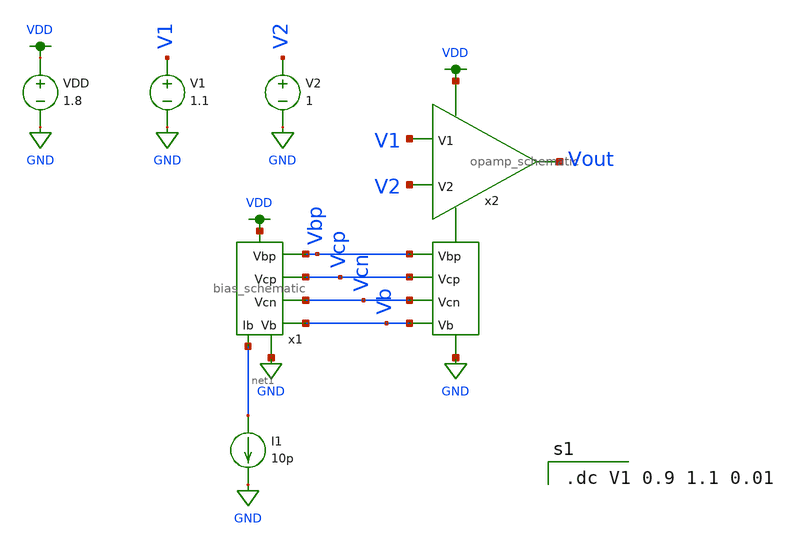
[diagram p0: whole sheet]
** sch_path: mp3/xschem/test_opamp.sch
**.subckt test_opamp
x1 VDD Vbp net1 Vcp Vcn GND Vb bias_schematic
x2 VDD Vbp Vcp Vout V1 V2 Vcn Vb GND opamp_schematic
I1 net1 GND 10p
V1 V1 GND 1.1
V2 V2 GND 1
VDD VDD GND 1.8
**** begin user architecture code

.option wnflag=1
.lib ~/skywater/skywater-pdk/libraries/sky130_fd_pr_ngspice/latest/models/sky130.lib.spice tt


.dc V1 0.9 1.1 0.01

**** end user architecture code
**.ends

* expanding   symbol:  /home/madvlsi/dev/git/vlsi/mp3/xschem/bias_schematic.sym # of pins=7
** sym_path: mp3/debug_files/bias_schematic.sym
** sch_path: mp3/debug_files/bias_schematic.sch
.subckt bias_schematic VP Vbp Ib Vcp Vcn VN Vb
*.iopin VP
*.iopin VN
*.iopin Ib
*.opin Vcp
*.opin Vbp
*.opin Vcn
*.opin Vb
XM1a net2 net2 net1 GND sky130_fd_pr__nfet_01v8 L=0.5 W=30 nf=1 ad='int((nf+1)/2) * W/nf * 0.29' as='int((nf+2)/2) * W/nf * 0.29'
+ pd='2*int((nf+1)/2) * (W/nf + 0.29)' ps='2*int((nf+2)/2) * (W/nf + 0.29)' nrd='0.29 / W' nrs='0.29 / W'
+ sa=0 sb=0 sd=0 mult=1 m=1
XM1b net2 net2 net1 GND sky130_fd_pr__nfet_01v8 L=0.5 W=30 nf=1 ad='int((nf+1)/2) * W/nf * 0.29' as='int((nf+2)/2) * W/nf * 0.29'
+ pd='2*int((nf+1)/2) * (W/nf + 0.29)' ps='2*int((nf+2)/2) * (W/nf + 0.29)' nrd='0.29 / W' nrs='0.29 / W'
+ sa=0 sb=0 sd=0 mult=1 m=1
XM1c net2 net2 net1 GND sky130_fd_pr__nfet_01v8 L=0.5 W=30 nf=1 ad='int((nf+1)/2) * W/nf * 0.29' as='int((nf+2)/2) * W/nf * 0.29'
+ pd='2*int((nf+1)/2) * (W/nf + 0.29)' ps='2*int((nf+2)/2) * (W/nf + 0.29)' nrd='0.29 / W' nrs='0.29 / W'
+ sa=0 sb=0 sd=0 mult=1 m=1
XM1d net2 net2 net1 GND sky130_fd_pr__nfet_01v8 L=0.5 W=30 nf=1 ad='int((nf+1)/2) * W/nf * 0.29' as='int((nf+2)/2) * W/nf * 0.29'
+ pd='2*int((nf+1)/2) * (W/nf + 0.29)' ps='2*int((nf+2)/2) * (W/nf + 0.29)' nrd='0.29 / W' nrs='0.29 / W'
+ sa=0 sb=0 sd=0 mult=1 m=1
XM2a VN net2 net1 GND sky130_fd_pr__nfet_01v8 L=0.5 W=3 nf=1 ad='int((nf+1)/2) * W/nf * 0.29' as='int((nf+2)/2) * W/nf * 0.29'
+ pd='2*int((nf+1)/2) * (W/nf + 0.29)' ps='2*int((nf+2)/2) * (W/nf + 0.29)' nrd='0.29 / W' nrs='0.29 / W'
+ sa=0 sb=0 sd=0 mult=1 m=1
XM2b VN net2 net1 GND sky130_fd_pr__nfet_01v8 L=0.5 W=3 nf=1 ad='int((nf+1)/2) * W/nf * 0.29' as='int((nf+2)/2) * W/nf * 0.29'
+ pd='2*int((nf+1)/2) * (W/nf + 0.29)' ps='2*int((nf+2)/2) * (W/nf + 0.29)' nrd='0.29 / W' nrs='0.29 / W'
+ sa=0 sb=0 sd=0 mult=1 m=1
XM2c VN net2 net1 GND sky130_fd_pr__nfet_01v8 L=0.5 W=3 nf=1 ad='int((nf+1)/2) * W/nf * 0.29' as='int((nf+2)/2) * W/nf * 0.29'
+ pd='2*int((nf+1)/2) * (W/nf + 0.29)' ps='2*int((nf+2)/2) * (W/nf + 0.29)' nrd='0.29 / W' nrs='0.29 / W'
+ sa=0 sb=0 sd=0 mult=1 m=1
XM2d VN net2 net1 GND sky130_fd_pr__nfet_01v8 L=0.5 W=3 nf=1 ad='int((nf+1)/2) * W/nf * 0.29' as='int((nf+2)/2) * W/nf * 0.29'
+ pd='2*int((nf+1)/2) * (W/nf + 0.29)' ps='2*int((nf+2)/2) * (W/nf + 0.29)' nrd='0.29 / W' nrs='0.29 / W'
+ sa=0 sb=0 sd=0 mult=1 m=1
XM3a net2 Ib VP VDD sky130_fd_pr__pfet_01v8 L=0.5 W=3 nf=1 ad='int((nf+1)/2) * W/nf * 0.29' as='int((nf+2)/2) * W/nf * 0.29'
+ pd='2*int((nf+1)/2) * (W/nf + 0.29)' ps='2*int((nf+2)/2) * (W/nf + 0.29)' nrd='0.29 / W' nrs='0.29 / W'
+ sa=0 sb=0 sd=0 mult=1 m=1
XM3b net2 Ib VP VDD sky130_fd_pr__pfet_01v8 L=0.5 W=3 nf=1 ad='int((nf+1)/2) * W/nf * 0.29' as='int((nf+2)/2) * W/nf * 0.29'
+ pd='2*int((nf+1)/2) * (W/nf + 0.29)' ps='2*int((nf+2)/2) * (W/nf + 0.29)' nrd='0.29 / W' nrs='0.29 / W'
+ sa=0 sb=0 sd=0 mult=1 m=1
XM3c net2 Ib VP VDD sky130_fd_pr__pfet_01v8 L=0.5 W=3 nf=1 ad='int((nf+1)/2) * W/nf * 0.29' as='int((nf+2)/2) * W/nf * 0.29'
+ pd='2*int((nf+1)/2) * (W/nf + 0.29)' ps='2*int((nf+2)/2) * (W/nf + 0.29)' nrd='0.29 / W' nrs='0.29 / W'
+ sa=0 sb=0 sd=0 mult=1 m=1
XM3d net2 Ib VP VDD sky130_fd_pr__pfet_01v8 L=0.5 W=3 nf=1 ad='int((nf+1)/2) * W/nf * 0.29' as='int((nf+2)/2) * W/nf * 0.29'
+ pd='2*int((nf+1)/2) * (W/nf + 0.29)' ps='2*int((nf+2)/2) * (W/nf + 0.29)' nrd='0.29 / W' nrs='0.29 / W'
+ sa=0 sb=0 sd=0 mult=1 m=1
XM4a Vcn Ib VP VDD sky130_fd_pr__pfet_01v8 L=0.5 W=30 nf=1 ad='int((nf+1)/2) * W/nf * 0.29' as='int((nf+2)/2) * W/nf * 0.29'
+ pd='2*int((nf+1)/2) * (W/nf + 0.29)' ps='2*int((nf+2)/2) * (W/nf + 0.29)' nrd='0.29 / W' nrs='0.29 / W'
+ sa=0 sb=0 sd=0 mult=1 m=1
XM4b Vcn Ib VP VDD sky130_fd_pr__pfet_01v8 L=0.5 W=30 nf=1 ad='int((nf+1)/2) * W/nf * 0.29' as='int((nf+2)/2) * W/nf * 0.29'
+ pd='2*int((nf+1)/2) * (W/nf + 0.29)' ps='2*int((nf+2)/2) * (W/nf + 0.29)' nrd='0.29 / W' nrs='0.29 / W'
+ sa=0 sb=0 sd=0 mult=1 m=1
XM4c Vcn Ib VP VDD sky130_fd_pr__pfet_01v8 L=0.5 W=30 nf=1 ad='int((nf+1)/2) * W/nf * 0.29' as='int((nf+2)/2) * W/nf * 0.29'
+ pd='2*int((nf+1)/2) * (W/nf + 0.29)' ps='2*int((nf+2)/2) * (W/nf + 0.29)' nrd='0.29 / W' nrs='0.29 / W'
+ sa=0 sb=0 sd=0 mult=1 m=1
XM4d Vcn Ib VP VDD sky130_fd_pr__pfet_01v8 L=0.5 W=30 nf=1 ad='int((nf+1)/2) * W/nf * 0.29' as='int((nf+2)/2) * W/nf * 0.29'
+ pd='2*int((nf+1)/2) * (W/nf + 0.29)' ps='2*int((nf+2)/2) * (W/nf + 0.29)' nrd='0.29 / W' nrs='0.29 / W'
+ sa=0 sb=0 sd=0 mult=1 m=1
XM11a Ib Ib VP VDD sky130_fd_pr__pfet_01v8 L=0.5 W=3 nf=1 ad='int((nf+1)/2) * W/nf * 0.29' as='int((nf+2)/2) * W/nf * 0.29'
+ pd='2*int((nf+1)/2) * (W/nf + 0.29)' ps='2*int((nf+2)/2) * (W/nf + 0.29)' nrd='0.29 / W' nrs='0.29 / W'
+ sa=0 sb=0 sd=0 mult=1 m=1
XM11b Ib Ib VP VDD sky130_fd_pr__pfet_01v8 L=0.5 W=3 nf=1 ad='int((nf+1)/2) * W/nf * 0.29' as='int((nf+2)/2) * W/nf * 0.29'
+ pd='2*int((nf+1)/2) * (W/nf + 0.29)' ps='2*int((nf+2)/2) * (W/nf + 0.29)' nrd='0.29 / W' nrs='0.29 / W'
+ sa=0 sb=0 sd=0 mult=1 m=1
XM11c Ib Ib VP VDD sky130_fd_pr__pfet_01v8 L=0.5 W=3 nf=1 ad='int((nf+1)/2) * W/nf * 0.29' as='int((nf+2)/2) * W/nf * 0.29'
+ pd='2*int((nf+1)/2) * (W/nf + 0.29)' ps='2*int((nf+2)/2) * (W/nf + 0.29)' nrd='0.29 / W' nrs='0.29 / W'
+ sa=0 sb=0 sd=0 mult=1 m=1
XM11d Ib Ib VP VDD sky130_fd_pr__pfet_01v8 L=0.5 W=3 nf=1 ad='int((nf+1)/2) * W/nf * 0.29' as='int((nf+2)/2) * W/nf * 0.29'
+ pd='2*int((nf+1)/2) * (W/nf + 0.29)' ps='2*int((nf+2)/2) * (W/nf + 0.29)' nrd='0.29 / W' nrs='0.29 / W'
+ sa=0 sb=0 sd=0 mult=1 m=1
XM5a net1 Vcn Vcn GND sky130_fd_pr__nfet_01v8 L=0.5 W=30 nf=1 ad='int((nf+1)/2) * W/nf * 0.29' as='int((nf+2)/2) * W/nf * 0.29'
+ pd='2*int((nf+1)/2) * (W/nf + 0.29)' ps='2*int((nf+2)/2) * (W/nf + 0.29)' nrd='0.29 / W' nrs='0.29 / W'
+ sa=0 sb=0 sd=0 mult=1 m=1
XM5b net1 Vcn Vcn GND sky130_fd_pr__nfet_01v8 L=0.5 W=30 nf=1 ad='int((nf+1)/2) * W/nf * 0.29' as='int((nf+2)/2) * W/nf * 0.29'
+ pd='2*int((nf+1)/2) * (W/nf + 0.29)' ps='2*int((nf+2)/2) * (W/nf + 0.29)' nrd='0.29 / W' nrs='0.29 / W'
+ sa=0 sb=0 sd=0 mult=1 m=1
XM5c net1 Vcn Vcn GND sky130_fd_pr__nfet_01v8 L=0.5 W=30 nf=1 ad='int((nf+1)/2) * W/nf * 0.29' as='int((nf+2)/2) * W/nf * 0.29'
+ pd='2*int((nf+1)/2) * (W/nf + 0.29)' ps='2*int((nf+2)/2) * (W/nf + 0.29)' nrd='0.29 / W' nrs='0.29 / W'
+ sa=0 sb=0 sd=0 mult=1 m=1
XM5d net1 Vcn Vcn GND sky130_fd_pr__nfet_01v8 L=0.5 W=30 nf=1 ad='int((nf+1)/2) * W/nf * 0.29' as='int((nf+2)/2) * W/nf * 0.29'
+ pd='2*int((nf+1)/2) * (W/nf + 0.29)' ps='2*int((nf+2)/2) * (W/nf + 0.29)' nrd='0.29 / W' nrs='0.29 / W'
+ sa=0 sb=0 sd=0 mult=1 m=1
XM8a VN Vb net3 GND sky130_fd_pr__nfet_01v8 L=0.5 W=3 nf=1 ad='int((nf+1)/2) * W/nf * 0.29' as='int((nf+2)/2) * W/nf * 0.29'
+ pd='2*int((nf+1)/2) * (W/nf + 0.29)' ps='2*int((nf+2)/2) * (W/nf + 0.29)' nrd='0.29 / W' nrs='0.29 / W'
+ sa=0 sb=0 sd=0 mult=1 m=1
XM8b VN Vb net3 GND sky130_fd_pr__nfet_01v8 L=0.5 W=3 nf=1 ad='int((nf+1)/2) * W/nf * 0.29' as='int((nf+2)/2) * W/nf * 0.29'
+ pd='2*int((nf+1)/2) * (W/nf + 0.29)' ps='2*int((nf+2)/2) * (W/nf + 0.29)' nrd='0.29 / W' nrs='0.29 / W'
+ sa=0 sb=0 sd=0 mult=1 m=1
XM8c VN Vb net3 GND sky130_fd_pr__nfet_01v8 L=0.5 W=3 nf=1 ad='int((nf+1)/2) * W/nf * 0.29' as='int((nf+2)/2) * W/nf * 0.29'
+ pd='2*int((nf+1)/2) * (W/nf + 0.29)' ps='2*int((nf+2)/2) * (W/nf + 0.29)' nrd='0.29 / W' nrs='0.29 / W'
+ sa=0 sb=0 sd=0 mult=1 m=1
XM8d VN Vb net3 GND sky130_fd_pr__nfet_01v8 L=0.5 W=3 nf=1 ad='int((nf+1)/2) * W/nf * 0.29' as='int((nf+2)/2) * W/nf * 0.29'
+ pd='2*int((nf+1)/2) * (W/nf + 0.29)' ps='2*int((nf+2)/2) * (W/nf + 0.29)' nrd='0.29 / W' nrs='0.29 / W'
+ sa=0 sb=0 sd=0 mult=1 m=1
XM6a net3 net3 net4 VDD sky130_fd_pr__pfet_01v8 L=0.5 W=30 nf=1 ad='int((nf+1)/2) * W/nf * 0.29' as='int((nf+2)/2) * W/nf * 0.29'
+ pd='2*int((nf+1)/2) * (W/nf + 0.29)' ps='2*int((nf+2)/2) * (W/nf + 0.29)' nrd='0.29 / W' nrs='0.29 / W'
+ sa=0 sb=0 sd=0 mult=1 m=1
XM6b net3 net3 net4 VDD sky130_fd_pr__pfet_01v8 L=0.5 W=30 nf=1 ad='int((nf+1)/2) * W/nf * 0.29' as='int((nf+2)/2) * W/nf * 0.29'
+ pd='2*int((nf+1)/2) * (W/nf + 0.29)' ps='2*int((nf+2)/2) * (W/nf + 0.29)' nrd='0.29 / W' nrs='0.29 / W'
+ sa=0 sb=0 sd=0 mult=1 m=1
XM6c net3 net3 net4 VDD sky130_fd_pr__pfet_01v8 L=0.5 W=30 nf=1 ad='int((nf+1)/2) * W/nf * 0.29' as='int((nf+2)/2) * W/nf * 0.29'
+ pd='2*int((nf+1)/2) * (W/nf + 0.29)' ps='2*int((nf+2)/2) * (W/nf + 0.29)' nrd='0.29 / W' nrs='0.29 / W'
+ sa=0 sb=0 sd=0 mult=1 m=1
XM6d net3 net3 net4 VDD sky130_fd_pr__pfet_01v8 L=0.5 W=30 nf=1 ad='int((nf+1)/2) * W/nf * 0.29' as='int((nf+2)/2) * W/nf * 0.29'
+ pd='2*int((nf+1)/2) * (W/nf + 0.29)' ps='2*int((nf+2)/2) * (W/nf + 0.29)' nrd='0.29 / W' nrs='0.29 / W'
+ sa=0 sb=0 sd=0 mult=1 m=1
XM7a net4 net3 VP VDD sky130_fd_pr__pfet_01v8 L=0.5 W=3 nf=1 ad='int((nf+1)/2) * W/nf * 0.29' as='int((nf+2)/2) * W/nf * 0.29'
+ pd='2*int((nf+1)/2) * (W/nf + 0.29)' ps='2*int((nf+2)/2) * (W/nf + 0.29)' nrd='0.29 / W' nrs='0.29 / W'
+ sa=0 sb=0 sd=0 mult=1 m=1
XM7b net4 net3 VP VDD sky130_fd_pr__pfet_01v8 L=0.5 W=3 nf=1 ad='int((nf+1)/2) * W/nf * 0.29' as='int((nf+2)/2) * W/nf * 0.29'
+ pd='2*int((nf+1)/2) * (W/nf + 0.29)' ps='2*int((nf+2)/2) * (W/nf + 0.29)' nrd='0.29 / W' nrs='0.29 / W'
+ sa=0 sb=0 sd=0 mult=1 m=1
XM7c net4 net3 VP VDD sky130_fd_pr__pfet_01v8 L=0.5 W=3 nf=1 ad='int((nf+1)/2) * W/nf * 0.29' as='int((nf+2)/2) * W/nf * 0.29'
+ pd='2*int((nf+1)/2) * (W/nf + 0.29)' ps='2*int((nf+2)/2) * (W/nf + 0.29)' nrd='0.29 / W' nrs='0.29 / W'
+ sa=0 sb=0 sd=0 mult=1 m=1
XM7d net4 net3 VP VDD sky130_fd_pr__pfet_01v8 L=0.5 W=3 nf=1 ad='int((nf+1)/2) * W/nf * 0.29' as='int((nf+2)/2) * W/nf * 0.29'
+ pd='2*int((nf+1)/2) * (W/nf + 0.29)' ps='2*int((nf+2)/2) * (W/nf + 0.29)' nrd='0.29 / W' nrs='0.29 / W'
+ sa=0 sb=0 sd=0 mult=1 m=1
XM10d net4 Vcp Vcp VDD sky130_fd_pr__pfet_01v8 L=0.5 W=30 nf=1 ad='int((nf+1)/2) * W/nf * 0.29' as='int((nf+2)/2) * W/nf * 0.29'
+ pd='2*int((nf+1)/2) * (W/nf + 0.29)' ps='2*int((nf+2)/2) * (W/nf + 0.29)' nrd='0.29 / W' nrs='0.29 / W'
+ sa=0 sb=0 sd=0 mult=1 m=1
XM10c net4 Vcp Vcp VDD sky130_fd_pr__pfet_01v8 L=0.5 W=30 nf=1 ad='int((nf+1)/2) * W/nf * 0.29' as='int((nf+2)/2) * W/nf * 0.29'
+ pd='2*int((nf+1)/2) * (W/nf + 0.29)' ps='2*int((nf+2)/2) * (W/nf + 0.29)' nrd='0.29 / W' nrs='0.29 / W'
+ sa=0 sb=0 sd=0 mult=1 m=1
XM10b net4 Vcp Vcp VDD sky130_fd_pr__pfet_01v8 L=0.5 W=30 nf=1 ad='int((nf+1)/2) * W/nf * 0.29' as='int((nf+2)/2) * W/nf * 0.29'
+ pd='2*int((nf+1)/2) * (W/nf + 0.29)' ps='2*int((nf+2)/2) * (W/nf + 0.29)' nrd='0.29 / W' nrs='0.29 / W'
+ sa=0 sb=0 sd=0 mult=1 m=1
XM10a net4 Vcp Vcp VDD sky130_fd_pr__pfet_01v8 L=0.5 W=30 nf=1 ad='int((nf+1)/2) * W/nf * 0.29' as='int((nf+2)/2) * W/nf * 0.29'
+ pd='2*int((nf+1)/2) * (W/nf + 0.29)' ps='2*int((nf+2)/2) * (W/nf + 0.29)' nrd='0.29 / W' nrs='0.29 / W'
+ sa=0 sb=0 sd=0 mult=1 m=1
XM9a VN Vb Vcp GND sky130_fd_pr__nfet_01v8 L=0.5 W=30 nf=1 ad='int((nf+1)/2) * W/nf * 0.29' as='int((nf+2)/2) * W/nf * 0.29'
+ pd='2*int((nf+1)/2) * (W/nf + 0.29)' ps='2*int((nf+2)/2) * (W/nf + 0.29)' nrd='0.29 / W' nrs='0.29 / W'
+ sa=0 sb=0 sd=0 mult=1 m=1
XM9b VN Vb Vcp GND sky130_fd_pr__nfet_01v8 L=0.5 W=30 nf=1 ad='int((nf+1)/2) * W/nf * 0.29' as='int((nf+2)/2) * W/nf * 0.29'
+ pd='2*int((nf+1)/2) * (W/nf + 0.29)' ps='2*int((nf+2)/2) * (W/nf + 0.29)' nrd='0.29 / W' nrs='0.29 / W'
+ sa=0 sb=0 sd=0 mult=1 m=1
XM9c VN Vb Vcp GND sky130_fd_pr__nfet_01v8 L=0.5 W=30 nf=1 ad='int((nf+1)/2) * W/nf * 0.29' as='int((nf+2)/2) * W/nf * 0.29'
+ pd='2*int((nf+1)/2) * (W/nf + 0.29)' ps='2*int((nf+2)/2) * (W/nf + 0.29)' nrd='0.29 / W' nrs='0.29 / W'
+ sa=0 sb=0 sd=0 mult=1 m=1
XM9d VN Vb Vcp GND sky130_fd_pr__nfet_01v8 L=0.5 W=30 nf=1 ad='int((nf+1)/2) * W/nf * 0.29' as='int((nf+2)/2) * W/nf * 0.29'
+ pd='2*int((nf+1)/2) * (W/nf + 0.29)' ps='2*int((nf+2)/2) * (W/nf + 0.29)' nrd='0.29 / W' nrs='0.29 / W'
+ sa=0 sb=0 sd=0 mult=1 m=1
XM12a VN Vb Vb GND sky130_fd_pr__nfet_01v8 L=0.5 W=3 nf=1 ad='int((nf+1)/2) * W/nf * 0.29' as='int((nf+2)/2) * W/nf * 0.29'
+ pd='2*int((nf+1)/2) * (W/nf + 0.29)' ps='2*int((nf+2)/2) * (W/nf + 0.29)' nrd='0.29 / W' nrs='0.29 / W'
+ sa=0 sb=0 sd=0 mult=1 m=1
XM12b VN Vb Vb GND sky130_fd_pr__nfet_01v8 L=0.5 W=3 nf=1 ad='int((nf+1)/2) * W/nf * 0.29' as='int((nf+2)/2) * W/nf * 0.29'
+ pd='2*int((nf+1)/2) * (W/nf + 0.29)' ps='2*int((nf+2)/2) * (W/nf + 0.29)' nrd='0.29 / W' nrs='0.29 / W'
+ sa=0 sb=0 sd=0 mult=1 m=1
XM12c VN Vb Vb GND sky130_fd_pr__nfet_01v8 L=0.5 W=3 nf=1 ad='int((nf+1)/2) * W/nf * 0.29' as='int((nf+2)/2) * W/nf * 0.29'
+ pd='2*int((nf+1)/2) * (W/nf + 0.29)' ps='2*int((nf+2)/2) * (W/nf + 0.29)' nrd='0.29 / W' nrs='0.29 / W'
+ sa=0 sb=0 sd=0 mult=1 m=1
XM12d VN Vb Vb GND sky130_fd_pr__nfet_01v8 L=0.5 W=3 nf=1 ad='int((nf+1)/2) * W/nf * 0.29' as='int((nf+2)/2) * W/nf * 0.29'
+ pd='2*int((nf+1)/2) * (W/nf + 0.29)' ps='2*int((nf+2)/2) * (W/nf + 0.29)' nrd='0.29 / W' nrs='0.29 / W'
+ sa=0 sb=0 sd=0 mult=1 m=1
XM1 Vb Ib VP VDD sky130_fd_pr__pfet_01v8 L=0.5 W=3 nf=1 ad='int((nf+1)/2) * W/nf * 0.29' as='int((nf+2)/2) * W/nf * 0.29'
+ pd='2*int((nf+1)/2) * (W/nf + 0.29)' ps='2*int((nf+2)/2) * (W/nf + 0.29)' nrd='0.29 / W' nrs='0.29 / W'
+ sa=0 sb=0 sd=0 mult=1 m=1
XM2 Vb Ib VP VDD sky130_fd_pr__pfet_01v8 L=0.5 W=3 nf=1 ad='int((nf+1)/2) * W/nf * 0.29' as='int((nf+2)/2) * W/nf * 0.29'
+ pd='2*int((nf+1)/2) * (W/nf + 0.29)' ps='2*int((nf+2)/2) * (W/nf + 0.29)' nrd='0.29 / W' nrs='0.29 / W'
+ sa=0 sb=0 sd=0 mult=1 m=1
XM3 Vb Ib VP VDD sky130_fd_pr__pfet_01v8 L=0.5 W=3 nf=1 ad='int((nf+1)/2) * W/nf * 0.29' as='int((nf+2)/2) * W/nf * 0.29'
+ pd='2*int((nf+1)/2) * (W/nf + 0.29)' ps='2*int((nf+2)/2) * (W/nf + 0.29)' nrd='0.29 / W' nrs='0.29 / W'
+ sa=0 sb=0 sd=0 mult=1 m=1
XM4 Vb Ib VP VDD sky130_fd_pr__pfet_01v8 L=0.5 W=3 nf=1 ad='int((nf+1)/2) * W/nf * 0.29' as='int((nf+2)/2) * W/nf * 0.29'
+ pd='2*int((nf+1)/2) * (W/nf + 0.29)' ps='2*int((nf+2)/2) * (W/nf + 0.29)' nrd='0.29 / W' nrs='0.29 / W'
+ sa=0 sb=0 sd=0 mult=1 m=1
.ends


* expanding   symbol:  /home/madvlsi/dev/git/vlsi/mp3/xschem/opamp_schematic.sym # of pins=9
** sym_path: /home/madvlsi/dev/git/vlsi/mp3/xschem/opamp_schematic.sym
** sch_path: /home/madvlsi/dev/git/vlsi/mp3/xschem/opamp_schematic.sch
.subckt opamp_schematic VP Vbp Vcp Vout V1 V2 Vcn Vb VN
*.ipin Vbp
*.ipin Vcp
*.ipin Vcn
*.ipin V2
*.ipin V1
*.ipin Vb
*.iopin VP
*.iopin VN
*.opin Vout
XM1a net2 V1 net1 GND sky130_fd_pr__nfet_01v8 L=0.5 W=3 nf=1 ad='int((nf+1)/2) * W/nf * 0.29' as='int((nf+2)/2) * W/nf * 0.29'
+ pd='2*int((nf+1)/2) * (W/nf + 0.29)' ps='2*int((nf+2)/2) * (W/nf + 0.29)' nrd='0.29 / W' nrs='0.29 / W'
+ sa=0 sb=0 sd=0 mult=1 m=1
XM1b net2 V1 net1 GND sky130_fd_pr__nfet_01v8 L=0.5 W=3 nf=1 ad='int((nf+1)/2) * W/nf * 0.29' as='int((nf+2)/2) * W/nf * 0.29'
+ pd='2*int((nf+1)/2) * (W/nf + 0.29)' ps='2*int((nf+2)/2) * (W/nf + 0.29)' nrd='0.29 / W' nrs='0.29 / W'
+ sa=0 sb=0 sd=0 mult=1 m=1
XM1c net2 V1 net1 GND sky130_fd_pr__nfet_01v8 L=0.5 W=3 nf=1 ad='int((nf+1)/2) * W/nf * 0.29' as='int((nf+2)/2) * W/nf * 0.29'
+ pd='2*int((nf+1)/2) * (W/nf + 0.29)' ps='2*int((nf+2)/2) * (W/nf + 0.29)' nrd='0.29 / W' nrs='0.29 / W'
+ sa=0 sb=0 sd=0 mult=1 m=1
XM1d net2 V1 net1 GND sky130_fd_pr__nfet_01v8 L=0.5 W=3 nf=1 ad='int((nf+1)/2) * W/nf * 0.29' as='int((nf+2)/2) * W/nf * 0.29'
+ pd='2*int((nf+1)/2) * (W/nf + 0.29)' ps='2*int((nf+2)/2) * (W/nf + 0.29)' nrd='0.29 / W' nrs='0.29 / W'
+ sa=0 sb=0 sd=0 mult=1 m=1
XM2a net3 V2 net1 GND sky130_fd_pr__nfet_01v8 L=0.5 W=3 nf=1 ad='int((nf+1)/2) * W/nf * 0.29' as='int((nf+2)/2) * W/nf * 0.29'
+ pd='2*int((nf+1)/2) * (W/nf + 0.29)' ps='2*int((nf+2)/2) * (W/nf + 0.29)' nrd='0.29 / W' nrs='0.29 / W'
+ sa=0 sb=0 sd=0 mult=1 m=1
XM2b net3 V2 net1 GND sky130_fd_pr__nfet_01v8 L=0.5 W=3 nf=1 ad='int((nf+1)/2) * W/nf * 0.29' as='int((nf+2)/2) * W/nf * 0.29'
+ pd='2*int((nf+1)/2) * (W/nf + 0.29)' ps='2*int((nf+2)/2) * (W/nf + 0.29)' nrd='0.29 / W' nrs='0.29 / W'
+ sa=0 sb=0 sd=0 mult=1 m=1
XM2c net3 V2 net1 GND sky130_fd_pr__nfet_01v8 L=0.5 W=3 nf=1 ad='int((nf+1)/2) * W/nf * 0.29' as='int((nf+2)/2) * W/nf * 0.29'
+ pd='2*int((nf+1)/2) * (W/nf + 0.29)' ps='2*int((nf+2)/2) * (W/nf + 0.29)' nrd='0.29 / W' nrs='0.29 / W'
+ sa=0 sb=0 sd=0 mult=1 m=1
XM2d net3 V2 net1 GND sky130_fd_pr__nfet_01v8 L=0.5 W=3 nf=1 ad='int((nf+1)/2) * W/nf * 0.29' as='int((nf+2)/2) * W/nf * 0.29'
+ pd='2*int((nf+1)/2) * (W/nf + 0.29)' ps='2*int((nf+2)/2) * (W/nf + 0.29)' nrd='0.29 / W' nrs='0.29 / W'
+ sa=0 sb=0 sd=0 mult=1 m=1
XMba net1 Vb VN GND sky130_fd_pr__nfet_01v8 L=0.5 W=1.5 nf=1 ad='int((nf+1)/2) * W/nf * 0.29' as='int((nf+2)/2) * W/nf * 0.29'
+ pd='2*int((nf+1)/2) * (W/nf + 0.29)' ps='2*int((nf+2)/2) * (W/nf + 0.29)' nrd='0.29 / W' nrs='0.29 / W'
+ sa=0 sb=0 sd=0 mult=1 m=1
XMbb net1 Vb VN GND sky130_fd_pr__nfet_01v8 L=0.5 W=1.5 nf=1 ad='int((nf+1)/2) * W/nf * 0.29' as='int((nf+2)/2) * W/nf * 0.29'
+ pd='2*int((nf+1)/2) * (W/nf + 0.29)' ps='2*int((nf+2)/2) * (W/nf + 0.29)' nrd='0.29 / W' nrs='0.29 / W'
+ sa=0 sb=0 sd=0 mult=1 m=1
XMbc net1 Vb VN GND sky130_fd_pr__nfet_01v8 L=0.5 W=1.5 nf=1 ad='int((nf+1)/2) * W/nf * 0.29' as='int((nf+2)/2) * W/nf * 0.29'
+ pd='2*int((nf+1)/2) * (W/nf + 0.29)' ps='2*int((nf+2)/2) * (W/nf + 0.29)' nrd='0.29 / W' nrs='0.29 / W'
+ sa=0 sb=0 sd=0 mult=1 m=1
XMbd net1 Vb VN GND sky130_fd_pr__nfet_01v8 L=0.5 W=1.5 nf=1 ad='int((nf+1)/2) * W/nf * 0.29' as='int((nf+2)/2) * W/nf * 0.29'
+ pd='2*int((nf+1)/2) * (W/nf + 0.29)' ps='2*int((nf+2)/2) * (W/nf + 0.29)' nrd='0.29 / W' nrs='0.29 / W'
+ sa=0 sb=0 sd=0 mult=1 m=1
XMbe net1 Vb VN GND sky130_fd_pr__nfet_01v8 L=0.5 W=1.5 nf=1 ad='int((nf+1)/2) * W/nf * 0.29' as='int((nf+2)/2) * W/nf * 0.29'
+ pd='2*int((nf+1)/2) * (W/nf + 0.29)' ps='2*int((nf+2)/2) * (W/nf + 0.29)' nrd='0.29 / W' nrs='0.29 / W'
+ sa=0 sb=0 sd=0 mult=1 m=1
XMbf net1 Vb VN GND sky130_fd_pr__nfet_01v8 L=0.5 W=1.5 nf=1 ad='int((nf+1)/2) * W/nf * 0.29' as='int((nf+2)/2) * W/nf * 0.29'
+ pd='2*int((nf+1)/2) * (W/nf + 0.29)' ps='2*int((nf+2)/2) * (W/nf + 0.29)' nrd='0.29 / W' nrs='0.29 / W'
+ sa=0 sb=0 sd=0 mult=1 m=1
XMbg net1 Vb VN GND sky130_fd_pr__nfet_01v8 L=0.5 W=1.5 nf=1 ad='int((nf+1)/2) * W/nf * 0.29' as='int((nf+2)/2) * W/nf * 0.29'
+ pd='2*int((nf+1)/2) * (W/nf + 0.29)' ps='2*int((nf+2)/2) * (W/nf + 0.29)' nrd='0.29 / W' nrs='0.29 / W'
+ sa=0 sb=0 sd=0 mult=1 m=1
XMbh net1 Vb VN GND sky130_fd_pr__nfet_01v8 L=0.5 W=1.5 nf=1 ad='int((nf+1)/2) * W/nf * 0.29' as='int((nf+2)/2) * W/nf * 0.29'
+ pd='2*int((nf+1)/2) * (W/nf + 0.29)' ps='2*int((nf+2)/2) * (W/nf + 0.29)' nrd='0.29 / W' nrs='0.29 / W'
+ sa=0 sb=0 sd=0 mult=1 m=1
XM7a net5 Vcn net4 GND sky130_fd_pr__nfet_01v8 L=0.5 W=3 nf=1 ad='int((nf+1)/2) * W/nf * 0.29' as='int((nf+2)/2) * W/nf * 0.29'
+ pd='2*int((nf+1)/2) * (W/nf + 0.29)' ps='2*int((nf+2)/2) * (W/nf + 0.29)' nrd='0.29 / W' nrs='0.29 / W'
+ sa=0 sb=0 sd=0 mult=1 m=1
XM7b net5 Vcn net4 GND sky130_fd_pr__nfet_01v8 L=0.5 W=3 nf=1 ad='int((nf+1)/2) * W/nf * 0.29' as='int((nf+2)/2) * W/nf * 0.29'
+ pd='2*int((nf+1)/2) * (W/nf + 0.29)' ps='2*int((nf+2)/2) * (W/nf + 0.29)' nrd='0.29 / W' nrs='0.29 / W'
+ sa=0 sb=0 sd=0 mult=1 m=1
XM7c net5 Vcn net4 GND sky130_fd_pr__nfet_01v8 L=0.5 W=3 nf=1 ad='int((nf+1)/2) * W/nf * 0.29' as='int((nf+2)/2) * W/nf * 0.29'
+ pd='2*int((nf+1)/2) * (W/nf + 0.29)' ps='2*int((nf+2)/2) * (W/nf + 0.29)' nrd='0.29 / W' nrs='0.29 / W'
+ sa=0 sb=0 sd=0 mult=1 m=1
XM7d net5 Vcn net4 GND sky130_fd_pr__nfet_01v8 L=0.5 W=3 nf=1 ad='int((nf+1)/2) * W/nf * 0.29' as='int((nf+2)/2) * W/nf * 0.29'
+ pd='2*int((nf+1)/2) * (W/nf + 0.29)' ps='2*int((nf+2)/2) * (W/nf + 0.29)' nrd='0.29 / W' nrs='0.29 / W'
+ sa=0 sb=0 sd=0 mult=1 m=1
XM8a net6 Vcn Vout GND sky130_fd_pr__nfet_01v8 L=0.5 W=3 nf=1 ad='int((nf+1)/2) * W/nf * 0.29' as='int((nf+2)/2) * W/nf * 0.29'
+ pd='2*int((nf+1)/2) * (W/nf + 0.29)' ps='2*int((nf+2)/2) * (W/nf + 0.29)' nrd='0.29 / W' nrs='0.29 / W'
+ sa=0 sb=0 sd=0 mult=1 m=1
XM8b net6 Vcn Vout GND sky130_fd_pr__nfet_01v8 L=0.5 W=3 nf=1 ad='int((nf+1)/2) * W/nf * 0.29' as='int((nf+2)/2) * W/nf * 0.29'
+ pd='2*int((nf+1)/2) * (W/nf + 0.29)' ps='2*int((nf+2)/2) * (W/nf + 0.29)' nrd='0.29 / W' nrs='0.29 / W'
+ sa=0 sb=0 sd=0 mult=1 m=1
XM8c net6 Vcn Vout GND sky130_fd_pr__nfet_01v8 L=0.5 W=3 nf=1 ad='int((nf+1)/2) * W/nf * 0.29' as='int((nf+2)/2) * W/nf * 0.29'
+ pd='2*int((nf+1)/2) * (W/nf + 0.29)' ps='2*int((nf+2)/2) * (W/nf + 0.29)' nrd='0.29 / W' nrs='0.29 / W'
+ sa=0 sb=0 sd=0 mult=1 m=1
XM8d net6 Vcn Vout GND sky130_fd_pr__nfet_01v8 L=0.5 W=3 nf=1 ad='int((nf+1)/2) * W/nf * 0.29' as='int((nf+2)/2) * W/nf * 0.29'
+ pd='2*int((nf+1)/2) * (W/nf + 0.29)' ps='2*int((nf+2)/2) * (W/nf + 0.29)' nrd='0.29 / W' nrs='0.29 / W'
+ sa=0 sb=0 sd=0 mult=1 m=1
XM9a net4 net5 VN GND sky130_fd_pr__nfet_01v8 L=0.5 W=3 nf=1 ad='int((nf+1)/2) * W/nf * 0.29' as='int((nf+2)/2) * W/nf * 0.29'
+ pd='2*int((nf+1)/2) * (W/nf + 0.29)' ps='2*int((nf+2)/2) * (W/nf + 0.29)' nrd='0.29 / W' nrs='0.29 / W'
+ sa=0 sb=0 sd=0 mult=1 m=1
XM9b net4 net5 VN GND sky130_fd_pr__nfet_01v8 L=0.5 W=3 nf=1 ad='int((nf+1)/2) * W/nf * 0.29' as='int((nf+2)/2) * W/nf * 0.29'
+ pd='2*int((nf+1)/2) * (W/nf + 0.29)' ps='2*int((nf+2)/2) * (W/nf + 0.29)' nrd='0.29 / W' nrs='0.29 / W'
+ sa=0 sb=0 sd=0 mult=1 m=1
XM9c net4 net5 VN GND sky130_fd_pr__nfet_01v8 L=0.5 W=3 nf=1 ad='int((nf+1)/2) * W/nf * 0.29' as='int((nf+2)/2) * W/nf * 0.29'
+ pd='2*int((nf+1)/2) * (W/nf + 0.29)' ps='2*int((nf+2)/2) * (W/nf + 0.29)' nrd='0.29 / W' nrs='0.29 / W'
+ sa=0 sb=0 sd=0 mult=1 m=1
XM9d net4 net5 VN GND sky130_fd_pr__nfet_01v8 L=0.5 W=3 nf=1 ad='int((nf+1)/2) * W/nf * 0.29' as='int((nf+2)/2) * W/nf * 0.29'
+ pd='2*int((nf+1)/2) * (W/nf + 0.29)' ps='2*int((nf+2)/2) * (W/nf + 0.29)' nrd='0.29 / W' nrs='0.29 / W'
+ sa=0 sb=0 sd=0 mult=1 m=1
XM10a VN net5 net6 GND sky130_fd_pr__nfet_01v8 L=0.5 W=3 nf=1 ad='int((nf+1)/2) * W/nf * 0.29' as='int((nf+2)/2) * W/nf * 0.29'
+ pd='2*int((nf+1)/2) * (W/nf + 0.29)' ps='2*int((nf+2)/2) * (W/nf + 0.29)' nrd='0.29 / W' nrs='0.29 / W'
+ sa=0 sb=0 sd=0 mult=1 m=1
XM10b VN net5 net6 GND sky130_fd_pr__nfet_01v8 L=0.5 W=3 nf=1 ad='int((nf+1)/2) * W/nf * 0.29' as='int((nf+2)/2) * W/nf * 0.29'
+ pd='2*int((nf+1)/2) * (W/nf + 0.29)' ps='2*int((nf+2)/2) * (W/nf + 0.29)' nrd='0.29 / W' nrs='0.29 / W'
+ sa=0 sb=0 sd=0 mult=1 m=1
XM10c VN net5 net6 GND sky130_fd_pr__nfet_01v8 L=0.5 W=3 nf=1 ad='int((nf+1)/2) * W/nf * 0.29' as='int((nf+2)/2) * W/nf * 0.29'
+ pd='2*int((nf+1)/2) * (W/nf + 0.29)' ps='2*int((nf+2)/2) * (W/nf + 0.29)' nrd='0.29 / W' nrs='0.29 / W'
+ sa=0 sb=0 sd=0 mult=1 m=1
XM1 VN net5 net6 GND sky130_fd_pr__nfet_01v8 L=0.5 W=3 nf=1 ad='int((nf+1)/2) * W/nf * 0.29' as='int((nf+2)/2) * W/nf * 0.29'
+ pd='2*int((nf+1)/2) * (W/nf + 0.29)' ps='2*int((nf+2)/2) * (W/nf + 0.29)' nrd='0.29 / W' nrs='0.29 / W'
+ sa=0 sb=0 sd=0 mult=1 m=1
XM5a net5 Vcp net2 VDD sky130_fd_pr__pfet_01v8 L=0.5 W=3 nf=1 ad='int((nf+1)/2) * W/nf * 0.29' as='int((nf+2)/2) * W/nf * 0.29'
+ pd='2*int((nf+1)/2) * (W/nf + 0.29)' ps='2*int((nf+2)/2) * (W/nf + 0.29)' nrd='0.29 / W' nrs='0.29 / W'
+ sa=0 sb=0 sd=0 mult=1 m=1
XM5b net5 Vcp net2 VDD sky130_fd_pr__pfet_01v8 L=0.5 W=3 nf=1 ad='int((nf+1)/2) * W/nf * 0.29' as='int((nf+2)/2) * W/nf * 0.29'
+ pd='2*int((nf+1)/2) * (W/nf + 0.29)' ps='2*int((nf+2)/2) * (W/nf + 0.29)' nrd='0.29 / W' nrs='0.29 / W'
+ sa=0 sb=0 sd=0 mult=1 m=1
XM5c net5 Vcp net2 VDD sky130_fd_pr__pfet_01v8 L=0.5 W=3 nf=1 ad='int((nf+1)/2) * W/nf * 0.29' as='int((nf+2)/2) * W/nf * 0.29'
+ pd='2*int((nf+1)/2) * (W/nf + 0.29)' ps='2*int((nf+2)/2) * (W/nf + 0.29)' nrd='0.29 / W' nrs='0.29 / W'
+ sa=0 sb=0 sd=0 mult=1 m=1
XM5d net5 Vcp net2 VDD sky130_fd_pr__pfet_01v8 L=0.5 W=3 nf=1 ad='int((nf+1)/2) * W/nf * 0.29' as='int((nf+2)/2) * W/nf * 0.29'
+ pd='2*int((nf+1)/2) * (W/nf + 0.29)' ps='2*int((nf+2)/2) * (W/nf + 0.29)' nrd='0.29 / W' nrs='0.29 / W'
+ sa=0 sb=0 sd=0 mult=1 m=1
XM6a Vout Vcp net3 VDD sky130_fd_pr__pfet_01v8 L=0.5 W=3 nf=1 ad='int((nf+1)/2) * W/nf * 0.29' as='int((nf+2)/2) * W/nf * 0.29'
+ pd='2*int((nf+1)/2) * (W/nf + 0.29)' ps='2*int((nf+2)/2) * (W/nf + 0.29)' nrd='0.29 / W' nrs='0.29 / W'
+ sa=0 sb=0 sd=0 mult=1 m=1
XM6b Vout Vcp net3 VDD sky130_fd_pr__pfet_01v8 L=0.5 W=3 nf=1 ad='int((nf+1)/2) * W/nf * 0.29' as='int((nf+2)/2) * W/nf * 0.29'
+ pd='2*int((nf+1)/2) * (W/nf + 0.29)' ps='2*int((nf+2)/2) * (W/nf + 0.29)' nrd='0.29 / W' nrs='0.29 / W'
+ sa=0 sb=0 sd=0 mult=1 m=1
XM6c Vout Vcp net3 VDD sky130_fd_pr__pfet_01v8 L=0.5 W=3 nf=1 ad='int((nf+1)/2) * W/nf * 0.29' as='int((nf+2)/2) * W/nf * 0.29'
+ pd='2*int((nf+1)/2) * (W/nf + 0.29)' ps='2*int((nf+2)/2) * (W/nf + 0.29)' nrd='0.29 / W' nrs='0.29 / W'
+ sa=0 sb=0 sd=0 mult=1 m=1
XM6d Vout Vcp net3 VDD sky130_fd_pr__pfet_01v8 L=0.5 W=3 nf=1 ad='int((nf+1)/2) * W/nf * 0.29' as='int((nf+2)/2) * W/nf * 0.29'
+ pd='2*int((nf+1)/2) * (W/nf + 0.29)' ps='2*int((nf+2)/2) * (W/nf + 0.29)' nrd='0.29 / W' nrs='0.29 / W'
+ sa=0 sb=0 sd=0 mult=1 m=1
XM3a net2 Vbp VP VDD sky130_fd_pr__pfet_01v8 L=0.5 W=3 nf=1 ad='int((nf+1)/2) * W/nf * 0.29' as='int((nf+2)/2) * W/nf * 0.29'
+ pd='2*int((nf+1)/2) * (W/nf + 0.29)' ps='2*int((nf+2)/2) * (W/nf + 0.29)' nrd='0.29 / W' nrs='0.29 / W'
+ sa=0 sb=0 sd=0 mult=1 m=1
XM3b net2 Vbp VP VDD sky130_fd_pr__pfet_01v8 L=0.5 W=3 nf=1 ad='int((nf+1)/2) * W/nf * 0.29' as='int((nf+2)/2) * W/nf * 0.29'
+ pd='2*int((nf+1)/2) * (W/nf + 0.29)' ps='2*int((nf+2)/2) * (W/nf + 0.29)' nrd='0.29 / W' nrs='0.29 / W'
+ sa=0 sb=0 sd=0 mult=1 m=1
XM3c net2 Vbp VP VDD sky130_fd_pr__pfet_01v8 L=0.5 W=3 nf=1 ad='int((nf+1)/2) * W/nf * 0.29' as='int((nf+2)/2) * W/nf * 0.29'
+ pd='2*int((nf+1)/2) * (W/nf + 0.29)' ps='2*int((nf+2)/2) * (W/nf + 0.29)' nrd='0.29 / W' nrs='0.29 / W'
+ sa=0 sb=0 sd=0 mult=1 m=1
XM3d net2 Vbp VP VDD sky130_fd_pr__pfet_01v8 L=0.5 W=3 nf=1 ad='int((nf+1)/2) * W/nf * 0.29' as='int((nf+2)/2) * W/nf * 0.29'
+ pd='2*int((nf+1)/2) * (W/nf + 0.29)' ps='2*int((nf+2)/2) * (W/nf + 0.29)' nrd='0.29 / W' nrs='0.29 / W'
+ sa=0 sb=0 sd=0 mult=1 m=1
XM4a net3 Vbp VP VDD sky130_fd_pr__pfet_01v8 L=0.5 W=3 nf=1 ad='int((nf+1)/2) * W/nf * 0.29' as='int((nf+2)/2) * W/nf * 0.29'
+ pd='2*int((nf+1)/2) * (W/nf + 0.29)' ps='2*int((nf+2)/2) * (W/nf + 0.29)' nrd='0.29 / W' nrs='0.29 / W'
+ sa=0 sb=0 sd=0 mult=1 m=1
XM4b net3 Vbp VP VDD sky130_fd_pr__pfet_01v8 L=0.5 W=3 nf=1 ad='int((nf+1)/2) * W/nf * 0.29' as='int((nf+2)/2) * W/nf * 0.29'
+ pd='2*int((nf+1)/2) * (W/nf + 0.29)' ps='2*int((nf+2)/2) * (W/nf + 0.29)' nrd='0.29 / W' nrs='0.29 / W'
+ sa=0 sb=0 sd=0 mult=1 m=1
XM4c net3 Vbp VP VDD sky130_fd_pr__pfet_01v8 L=0.5 W=3 nf=1 ad='int((nf+1)/2) * W/nf * 0.29' as='int((nf+2)/2) * W/nf * 0.29'
+ pd='2*int((nf+1)/2) * (W/nf + 0.29)' ps='2*int((nf+2)/2) * (W/nf + 0.29)' nrd='0.29 / W' nrs='0.29 / W'
+ sa=0 sb=0 sd=0 mult=1 m=1
XM4d net3 Vbp VP VDD sky130_fd_pr__pfet_01v8 L=0.5 W=3 nf=1 ad='int((nf+1)/2) * W/nf * 0.29' as='int((nf+2)/2) * W/nf * 0.29'
+ pd='2*int((nf+1)/2) * (W/nf + 0.29)' ps='2*int((nf+2)/2) * (W/nf + 0.29)' nrd='0.29 / W' nrs='0.29 / W'
+ sa=0 sb=0 sd=0 mult=1 m=1
.ends

.GLOBAL VDD
.GLOBAL GND
.end
